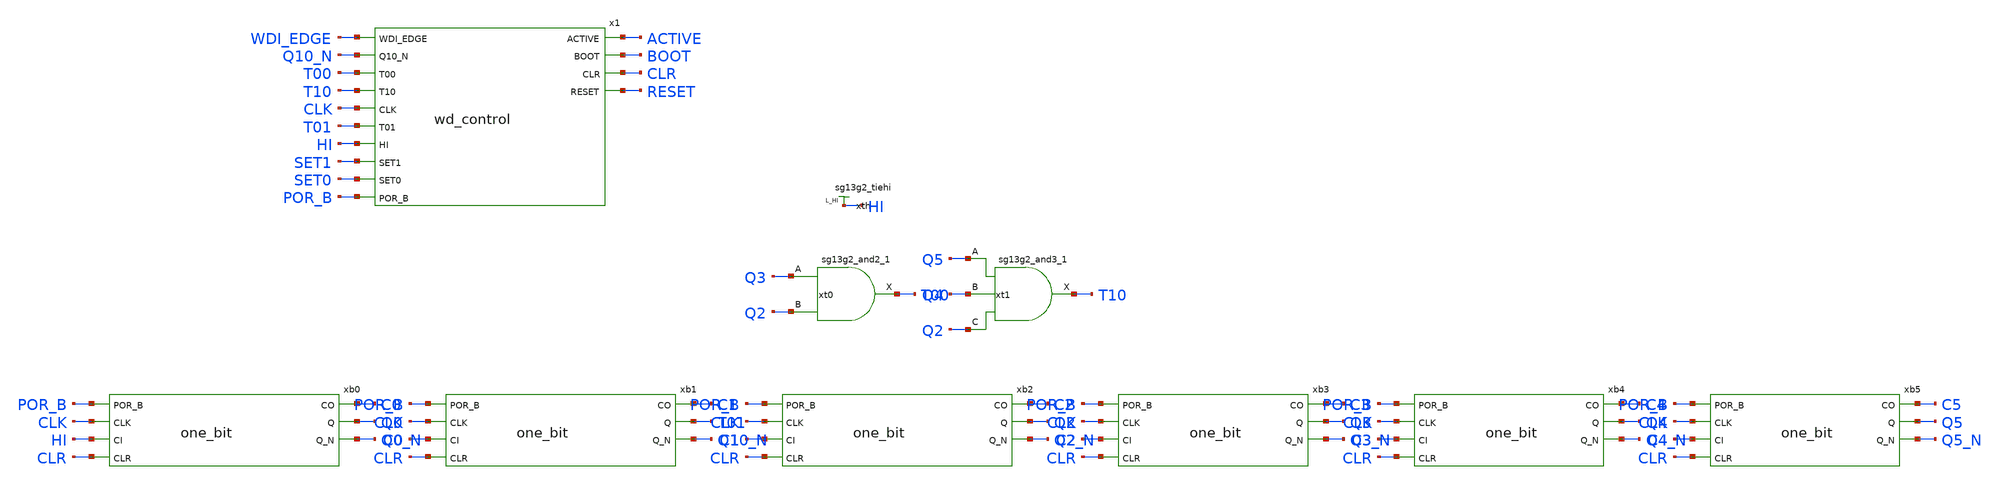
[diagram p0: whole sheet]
** sch_path: design/blocks/digital/schematic/wd_control_tb.sch
**.subckt wd_control_tb
x1 WDI_EDGE Q10_N T00 T10 CLK T01 HI ACTIVE SET1 BOOT CLR SET0 RESET POR_B VDD VSS wd_control
xb0 C0 POR_B CLK HI CLR Q0 Q0_N VDD VSS one_bit
xb1 C1 POR_B CLK C0 CLR T01 Q10_N VDD VSS one_bit
xb2 C2 POR_B CLK C1 CLR Q2 Q2_N VDD VSS one_bit
xb3 C3 POR_B CLK C2 CLR Q3 Q3_N VDD VSS one_bit
xb4 C4 POR_B CLK C3 CLR Q4 Q4_N VDD VSS one_bit
xb5 C5 POR_B CLK C4 CLR Q5 Q5_N VDD VSS one_bit
xt0 T00 Q3 Q2 VDD VSS sg13g2_and2_1
xt1 T10 Q5 Q4 Q2 VDD VSS sg13g2_and3_1
xth HI VDD VSS sg13g2_tiehi
**** begin user architecture code



.lib cornerMOSlv.lib mos_tt
.lib cornerMOShv.lib mos_tt
.lib cornerHBT.lib hbt_typ
.lib cornerRES.lib res_typ
.lib cornerDIO.lib dio_tt
.lib cornerCAP.lib cap_typ






* ============================================================
* wd_control_tb -- validacion a nivel transistor de wd_control (IHP SG13G2)
* Lazo cerrado con un contador ESCALADO de 6 bits hecho con one_bit (celdas reales):
*   T01 = Q1 (cuenta 2), T00 = Q3&Q2 (12), T10 = Q5&Q4&Q2 (52), Q10_N = Q1_N
*   -> pulso de reset 3 T, timeouts 13 / 3 / 53 T (SET = 00 / 01 / 10), arranque 53 T.
* Las constantes reales (1025 / 10241 / 102401 T) se verifican en Icarus con el
* netlist exportado (wd_control_logic_tb.v).
* Corner MOS: editar la linea .lib (mos_tt / mos_ss / ...)
* Barre T = -40/27/85 C  x  VDD = 1.08/1.2/1.32 V dentro de .control
* CLK 10 MHz: flancos de subida en 50n + k*100n; entradas cambian en 20n + k*100n.
* WDI_EDGE se da como pulsos de un ciclo (lo que entrega WDI_INPUT).
* Fases: A SET=00 (arranque sin WDI -> pulso -> WDI -> timeout normal)
*        B SET=01 (WDI en arranque -> timeout de 3 T; WDI en el ultimo ciclo es valido)
*        C SET=10 (WDI -> 53 T; SET cambiado en marcha a 11 no tiene efecto)
*        D SET=11 (deshabilitado, con WDI)
* Eventos esperados de RESET (subida/bajada, +-2 ns): 5350/5650, 7350/7650,
* 9050/9350, 15350/15650 ns; sin un quinto pulso. ACTIVE y BOOT en 6 instantes.
.global VDD VSS
.param vdd=1.2

* ---- contador escalado (6 x one_bit) y tomas: dibujados en el esquematico ----

* ---------- fuentes y cargas ----------
CRS RESET 0 10f
CAC ACTIVE 0 10f
CBT BOOT 0 10f
V_VDD VDD 0 PWL(0 0 100n {vdd})
V_VSS VSS 0 0
V_CLK CLK 0 PULSE(0 {vdd} 50n 0.1n 0.1n 50n 100n)
V_POR POR_B 0 PWL(0 0 120n 0 120.01n {vdd} 8020n {vdd} 8020.01n 0 8220n 0 8220.01n {vdd} 9720n {vdd}
+ 9720.01n 0 9920n 0 9920.01n {vdd} 15720n {vdd} 15720.01n 0 15920n 0 15920.01n {vdd})
V_S0 SET0 0 PWL(0 0 8020n 0 8020.01n {vdd} 9720n {vdd} 9720.01n 0 10520n 0 10520.01n {vdd} 15720n {vdd}
+ 15720.01n {vdd})
V_S1 SET1 0 PWL(0 0 9720n 0 9720.01n {vdd} 15720n {vdd} 15720.01n {vdd})
V_WDI WDI_EDGE 0 PWL(0 0 6020n 0 6020.01n {vdd} 6120n {vdd} 6120.01n 0 8420n 0 8420.01n {vdd} 8520n {vdd}
+ 8520.01n 0 8720n 0 8720.01n {vdd} 8820n {vdd} 8820.01n 0 10020n 0 10020.01n {vdd} 10120n {vdd} 10120.01n
+ 0 16520n 0 16520.01n {vdd} 16620n {vdd} 16620.01n 0)
.option method=gear maxord=2 reltol=1e-3
* guardar solo lo necesario: con todos los nodos ngspice acumula ~3 GB en 9 casos
.save v(clk) v(por_b) v(set0) v(set1) v(wdi_edge) v(active) v(boot) v(reset)
.control
set noaskquit
compose tlist values -40 27 85
compose vlist values 1.08 1.2 1.32
compose rexp values 5350n 7350n 9050n 15350n
compose fexp values 5650n 7650n 9350n 15650n
let npass = 0
let ncase = 0
let it = 0
while it lt 3
 let iv = 0
 while iv lt 3
  let tt = tlist[it]
  let vv = vlist[iv]
  alterparam vdd = $&vv
  reset
  option temp = $&tt
  tran 0.1n 21000n 0 0.5n
  let nt = length(time)
  let tend = time[nt-1]
  if tend lt 20990n
   echo REINTENTO T=$&tt VDD=$&vv (aborto en t=$&tend)
   reset
   option temp = $&tt
   tran 0.05n 21000n 0 0.25n
  end
  let vh = vv/2
  let ok = 0
  let k = 0
  while k lt 4
   let kk = k + 1
   let tr = -1
   let tf = -1
   meas tran tr WHEN v(reset)=$&vh RISE=$&kk
   meas tran tf WHEN v(reset)=$&vh FALL=$&kk
   let er = abs(tr - rexp[k]) lt 2n
   let ef = abs(tf - fexp[k]) lt 2n
   if er & ef
    let ok = ok + 1
   else
    echo   evento $&kk : subida=$&tr bajada=$&tf
   end
   let k = k + 1
  end
  let r5 = -1
  meas tran r5 WHEN v(reset)=$&vh RISE=5
  meas tran a03 FIND v(active) AT=300n
  meas tran b03 FIND v(boot) AT=300n
  meas tran b70 FIND v(boot) AT=7000n
  meas tran b79 FIND v(boot) AT=7900n
  meas tran a18 FIND v(active) AT=18000n
  meas tran a20 FIND v(active) AT=20500n
  let lv = (a03 gt vh) & (b03 gt vh) & (b70 lt vh) & (b79 gt vh) & (a18 lt vh) & (a20 lt vh)
  let pass = (ok eq 4) & (r5 lt 0) & lv
  if pass > 0.5
   echo CASO T=$&tt VDD=$&vv : PASS  4/4 eventos de RESET a +-2 ns, niveles ok
   let npass = npass + 1
  else
   echo CASO T=$&tt VDD=$&vv : FAIL  eventos=$&ok/4 sin5=$&r5 niveles=$&lv
  end
  set wr_singlescale
  wrdata wd_control_{$&tt}_{$&vv}.txt v(clk) v(por_b) v(set0) v(set1) v(wdi_edge) v(active) v(boot) v(reset)
  destroy all
  let ncase = ncase + 1
  let iv = iv + 1
 end
 let it = it + 1
end
echo ===============================================
echo RESUMEN: $&npass / $&ncase casos PASS
if npass eq ncase
 echo VEREDICTO: PASS
else
 echo VEREDICTO: FAIL
end
.endc
.end


**** end user architecture code
**.ends
.end
